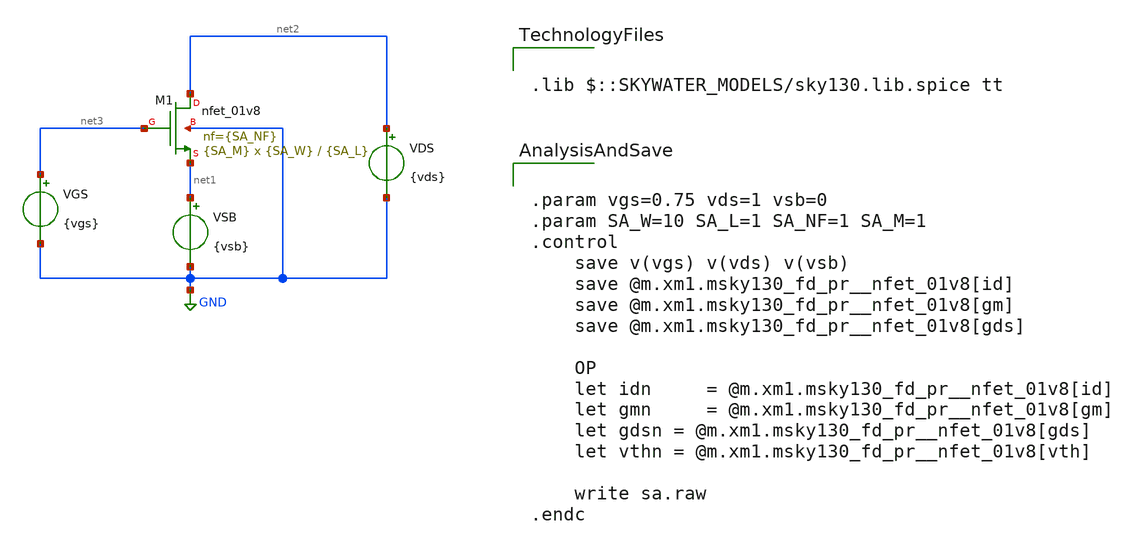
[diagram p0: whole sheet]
** sch_path: data/sa.sch
**.subckt sa
VGS net3 GND {vgs}
VDS net2 GND {vds}
VSB net1 GND {vsb}
XM1 net2 net3 net1 GND sky130_fd_pr__nfet_01v8 L={SA_L} W={SA_W} nf={SA_NF} ad='int((nf+1)/2) * W/nf * 0.29'
+ as='int((nf+2)/2) * W/nf * 0.29' pd='2*int((nf+1)/2) * (W/nf + 0.29)' ps='2*int((nf+2)/2) * (W/nf + 0.29)'
+ nrd='0.29 / W' nrs='0.29 / W' sa=0 sb=0 sd=0 mult={SA_M} m={SA_M}
**** begin user architecture code


.param vgs=0.75 vds=1 vsb=0
.param SA_W=10 SA_L=1 SA_NF=1 SA_M=1
.control
	save v(vgs) v(vds) v(vsb)
	save @m.xm1.msky130_fd_pr__nfet_01v8[id]
	save @m.xm1.msky130_fd_pr__nfet_01v8[gm]
	save @m.xm1.msky130_fd_pr__nfet_01v8[gds]

	OP
	let idn	 = @m.xm1.msky130_fd_pr__nfet_01v8[id]
	let gmn	 = @m.xm1.msky130_fd_pr__nfet_01v8[gm]
	let gdsn = @m.xm1.msky130_fd_pr__nfet_01v8[gds]
	let vthn = @m.xm1.msky130_fd_pr__nfet_01v8[vth]

	write sa.raw
.endc



.lib $::SKYWATER_MODELS/sky130.lib.spice tt

**** end user architecture code
**.ends
.GLOBAL GND
.end
